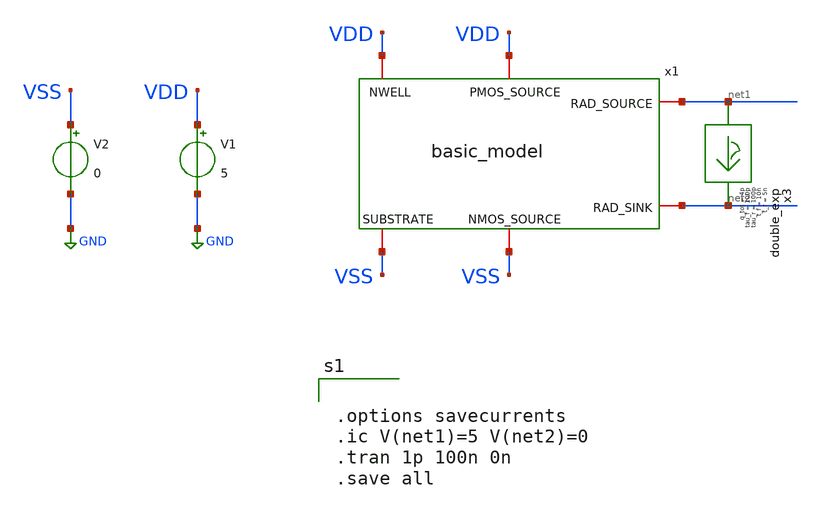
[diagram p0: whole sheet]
** sch_path: basic_test.sch
**.subckt basic_test
V1 VDD GND 5
V2 VSS GND 0
x3 net1 net2 double_exp t_r=5n tau_r=100p t_f=10n tau_f=100p q_tot=4p
x1 VDD VDD net1 net2 VSS VSS basic_model
**** begin user architecture code


.options savecurrents
.ic V(net1)=5 V(net2)=0
.tran 1p 100n 0n
.save all




.include /usr/local/share/rad_modeling_blocks/rad_modeling_blocks.spice


**** end user architecture code
**.ends

* expanding   symbol:  double_exp.sym # of pins=2
** sym_path: xschem_rad_library/double_exp.sym
** sch_path: xschem_rad_library/double_exp.sch
.subckt double_exp in out  t_r=0 t_f=0 tau_r=0 tau_f=0 q_tot=0
*.opin OUT
*.ipin IN
I1 IN OUT EXP(0 {q_tot / (t_f-t_r+tau_f-tau_r)} {t_r} {tau_r} {t_f} {tau_f})
.ends


* expanding   symbol:  OSCRE/latchup/basic_model.sym # of pins=6
** sym_path: latchup/basic_model.sym
** sch_path: latchup/basic_model.sch
.subckt basic_model PMOS_SOURCE NWELL RAD_SOURCE RAD_SINK NMOS_SOURCE SUBSTRATE   IS_N=1e-18
+  BF_N=100  VAF_N=50  IKF_N=0.01  CJE_N=0.2p  CJC_N=0.1p  TF_N=0.2n  TR_N=2n  IS_P=1e-18  BF_P=100  VAF_P=50
+  IKF_P=0.01  CJE_P=0.3p  CJC_P=0.15p  TF_P=0.3n  TR_P=3n
*.iopin NWELL
*.iopin SUBSTRATE
*.iopin RAD_SOURCE
*.iopin RAD_SINK
*.iopin NMOS_SOURCE
*.iopin PMOS_SOURCE
Q1 RAD_SINK RAD_SOURCE PMOS_SOURCE pnp_cust area=1 m=1
Q2 RAD_SOURCE RAD_SINK NMOS_SOURCE npn_cust area=1 m=1
R3 RAD_SINK SUBSTRATE 1000 m=1
R4 NWELL RAD_SOURCE 1000 m=1
**** begin user architecture code


.model npn_cust npn (IS={IS_N} BF={BF_N} VAF={VAF_N} IKF={IKF_N} CJE={CJE_N} CJC={CJC_N} TF={TF_N} TR={TR_N})
.model pnp_cust pnp (IS={IS_P} BF={BF_P} VAF={VAF_P} IKF={IKF_P} CJE={CJE_P} CJC={CJC_N} TF={TF_N} TR={TR_P})


**** end user architecture code
.ends

.GLOBAL GND
.end
